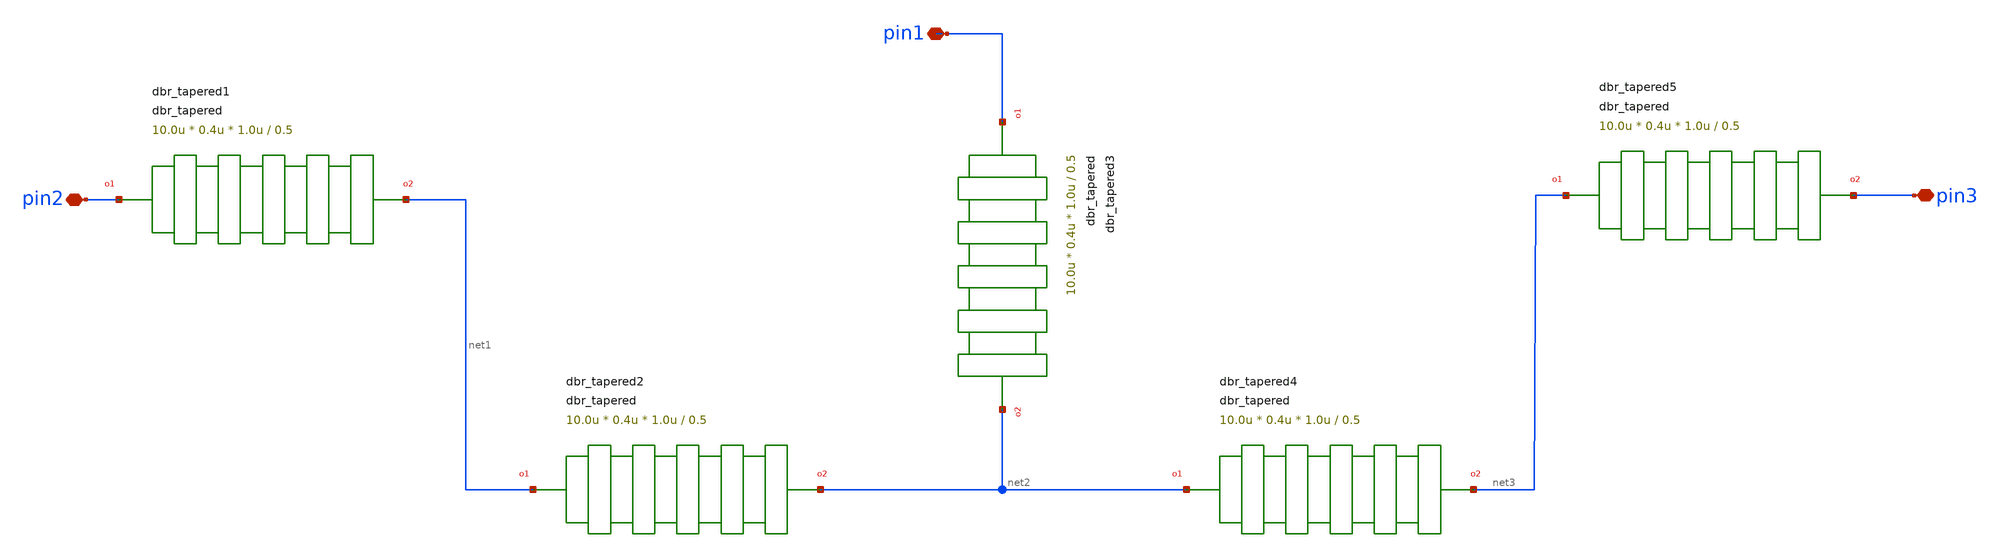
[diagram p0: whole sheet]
** sch_path: xschem/tests/test_sch/test_dbr_tapered.sch
* Copyright (c) 2024, Mabrains LLC
* Licensed under the GNU Lesser General Public License, Version 3.0 (the "License");
* you may not use this file except in compliance with the License.
* GNU Lesser General Public License
* Version 3, 29 June 2007
* This program is free software: you can redistribute it and/or modify
* it under the terms of the GNU Lesser General Public License as published
* by the Free Software Foundation, either version 3 of the License, or
* (at your option) any later version.
* This program is distributed in the hope that it will be useful,
* but WITHOUT ANY WARRANTY; without even the implied warranty of
* MERCHANTABILITY or FITNESS FOR A PARTICULAR PURPOSE.  See the
* GNU Lesser General Public License for more details.
* You should have received a copy of the GNU Lesser General Public License
* along with this program.  If not, see <https://www.gnu.org/licenses/>.
* SPDX-License-Identifier: LGPL-3.0
**.subckt test_dbr_tapered pin2 pin1 pin3
*.iopin pin2
*.iopin pin1
*.iopin pin3
Pdbr_tapered1 pin2 net1 dbr_tapered length=10.0u period=0.85 duty_cycle=0.5 w1=0.4u w2=1.0u
+ taper_length=20.0u
Pdbr_tapered2 net1 net2 dbr_tapered length=10.0u period=0.85 duty_cycle=0.5 w1=0.4u w2=1.0u
+ taper_length=20.0u
Pdbr_tapered3 pin1 net2 dbr_tapered length=10.0u period=0.85 duty_cycle=0.5 w1=0.4u w2=1.0u
+ taper_length=20.0u
Pdbr_tapered4 net2 net3 dbr_tapered length=10.0u period=0.85 duty_cycle=0.5 w1=0.4u w2=1.0u
+ taper_length=20.0u
Pdbr_tapered5 net3 pin3 dbr_tapered length=10.0u period=0.85 duty_cycle=0.5 w1=0.4u w2=1.0u
+ taper_length=20.0u
**.ends
.end
